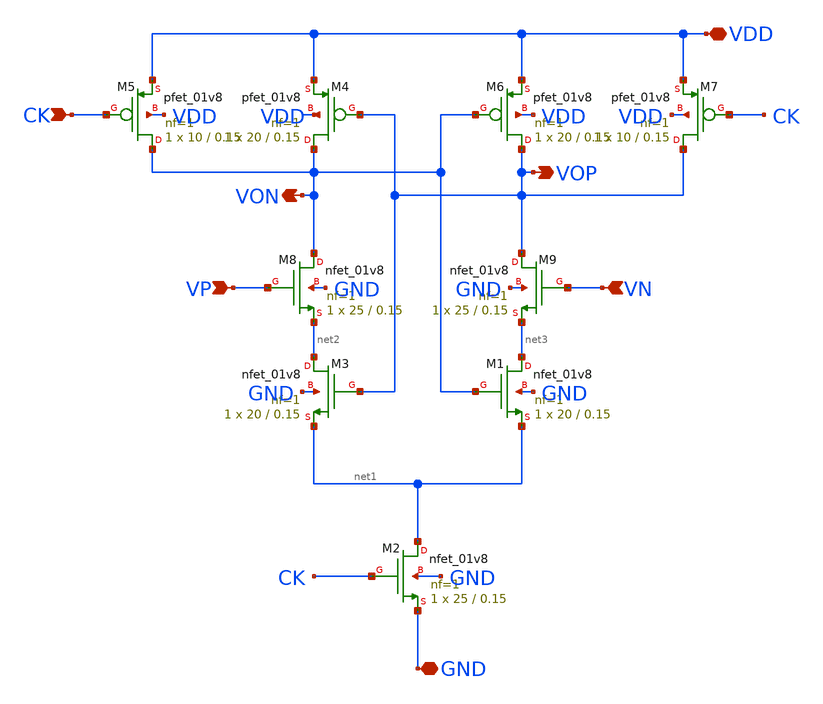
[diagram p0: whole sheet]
** sch_path: xschem/comparator.sch
**.subckt comparator GND VP VOP VON VN VDD CK
*.iopin GND
*.ipin VP
*.opin VOP
*.opin VON
*.ipin VN
*.iopin VDD
*.ipin CK
XM2 net1 CK GND GND sky130_fd_pr__nfet_01v8 L=0.15 W=25 nf=1 ad='int((nf+1)/2) * W/nf * 0.29' as='int((nf+2)/2) * W/nf * 0.29'
+ pd='2*int((nf+1)/2) * (W/nf + 0.29)' ps='2*int((nf+2)/2) * (W/nf + 0.29)' nrd='0.29 / W' nrs='0.29 / W'
+ sa=0 sb=0 sd=0 mult=1 m=1
XM3 net2 VOP net1 GND sky130_fd_pr__nfet_01v8 L=0.15 W=20 nf=1 ad='int((nf+1)/2) * W/nf * 0.29' as='int((nf+2)/2) * W/nf * 0.29'
+ pd='2*int((nf+1)/2) * (W/nf + 0.29)' ps='2*int((nf+2)/2) * (W/nf + 0.29)' nrd='0.29 / W' nrs='0.29 / W'
+ sa=0 sb=0 sd=0 mult=1 m=1
XM4 VON VOP VDD VDD sky130_fd_pr__pfet_01v8 L=0.15 W=20 nf=1 ad='int((nf+1)/2) * W/nf * 0.29' as='int((nf+2)/2) * W/nf * 0.29'
+ pd='2*int((nf+1)/2) * (W/nf + 0.29)' ps='2*int((nf+2)/2) * (W/nf + 0.29)' nrd='0.29 / W' nrs='0.29 / W'
+ sa=0 sb=0 sd=0 mult=1 m=1
XM5 VON CK VDD VDD sky130_fd_pr__pfet_01v8 L=0.15 W=10 nf=1 ad='int((nf+1)/2) * W/nf * 0.29' as='int((nf+2)/2) * W/nf * 0.29'
+ pd='2*int((nf+1)/2) * (W/nf + 0.29)' ps='2*int((nf+2)/2) * (W/nf + 0.29)' nrd='0.29 / W' nrs='0.29 / W'
+ sa=0 sb=0 sd=0 mult=1 m=1
XM1 net3 VON net1 GND sky130_fd_pr__nfet_01v8 L=0.15 W=20 nf=1 ad='int((nf+1)/2) * W/nf * 0.29' as='int((nf+2)/2) * W/nf * 0.29'
+ pd='2*int((nf+1)/2) * (W/nf + 0.29)' ps='2*int((nf+2)/2) * (W/nf + 0.29)' nrd='0.29 / W' nrs='0.29 / W'
+ sa=0 sb=0 sd=0 mult=1 m=1
XM6 VOP VON VDD VDD sky130_fd_pr__pfet_01v8 L=0.15 W=20 nf=1 ad='int((nf+1)/2) * W/nf * 0.29' as='int((nf+2)/2) * W/nf * 0.29'
+ pd='2*int((nf+1)/2) * (W/nf + 0.29)' ps='2*int((nf+2)/2) * (W/nf + 0.29)' nrd='0.29 / W' nrs='0.29 / W'
+ sa=0 sb=0 sd=0 mult=1 m=1
XM7 VOP CK VDD VDD sky130_fd_pr__pfet_01v8 L=0.15 W=10 nf=1 ad='int((nf+1)/2) * W/nf * 0.29' as='int((nf+2)/2) * W/nf * 0.29'
+ pd='2*int((nf+1)/2) * (W/nf + 0.29)' ps='2*int((nf+2)/2) * (W/nf + 0.29)' nrd='0.29 / W' nrs='0.29 / W'
+ sa=0 sb=0 sd=0 mult=1 m=1
XM8 VON VP net2 GND sky130_fd_pr__nfet_01v8 L=0.15 W=25 nf=1 ad='int((nf+1)/2) * W/nf * 0.29' as='int((nf+2)/2) * W/nf * 0.29'
+ pd='2*int((nf+1)/2) * (W/nf + 0.29)' ps='2*int((nf+2)/2) * (W/nf + 0.29)' nrd='0.29 / W' nrs='0.29 / W'
+ sa=0 sb=0 sd=0 mult=1 m=1
XM9 VOP VN net3 GND sky130_fd_pr__nfet_01v8 L=0.15 W=25 nf=1 ad='int((nf+1)/2) * W/nf * 0.29' as='int((nf+2)/2) * W/nf * 0.29'
+ pd='2*int((nf+1)/2) * (W/nf + 0.29)' ps='2*int((nf+2)/2) * (W/nf + 0.29)' nrd='0.29 / W' nrs='0.29 / W'
+ sa=0 sb=0 sd=0 mult=1 m=1
**.ends
.end
